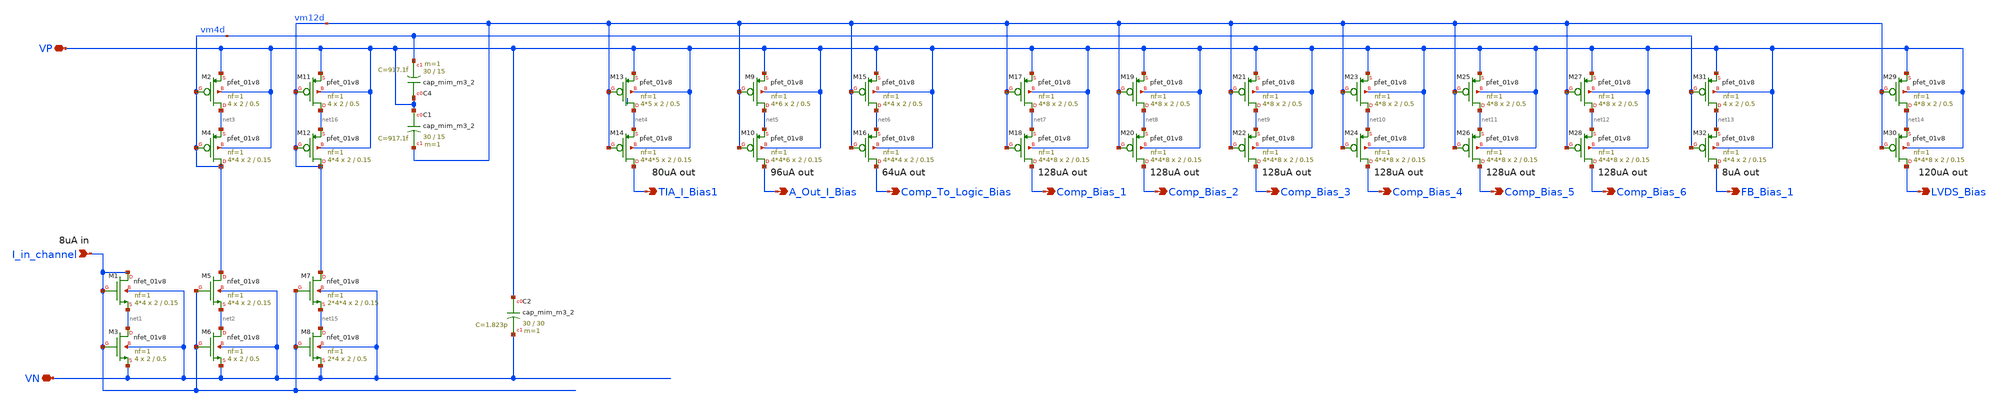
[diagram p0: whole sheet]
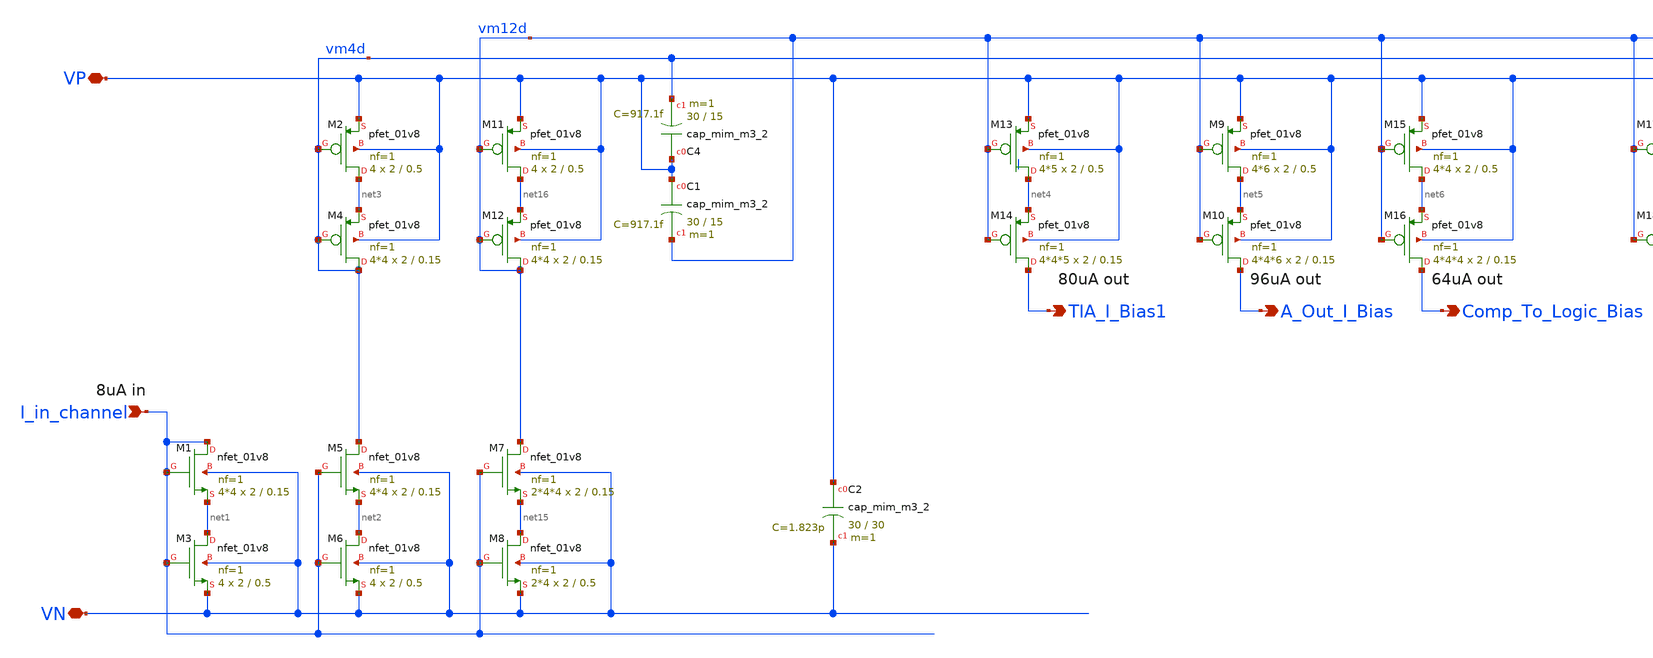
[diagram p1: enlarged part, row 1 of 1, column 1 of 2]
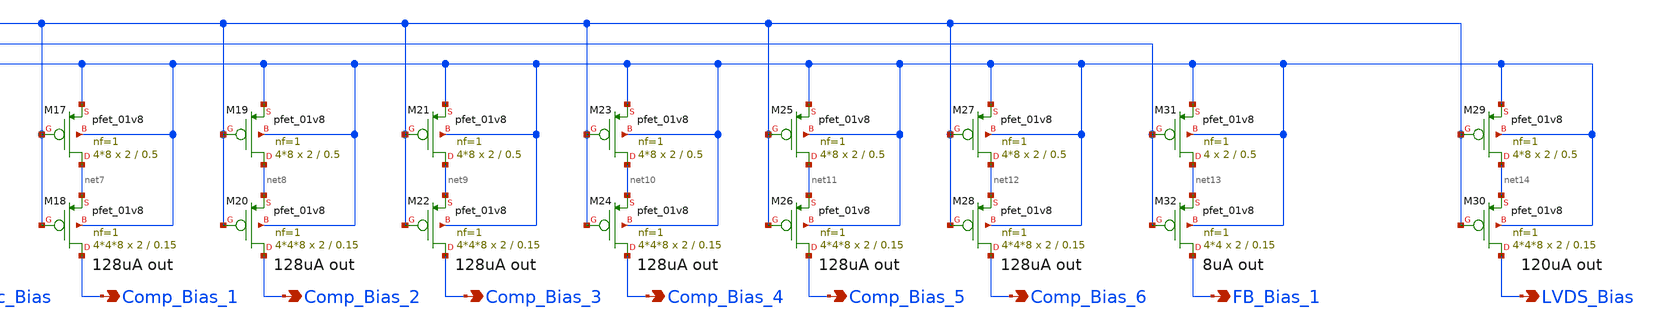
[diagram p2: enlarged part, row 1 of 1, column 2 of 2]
** sch_path: xschem/bias/current_mirror_channel.sch
**.subckt current_mirror_channel I_in_channel VP VN TIA_I_Bias1 A_Out_I_Bias Comp_Bias_1
*+ Comp_To_Logic_Bias Comp_Bias_2 Comp_Bias_3 Comp_Bias_4 Comp_Bias_5 Comp_Bias_6 FB_Bias_1 LVDS_Bias
*.ipin I_in_channel
*.iopin VP
*.iopin VN
*.opin TIA_I_Bias1
*.opin A_Out_I_Bias
*.opin Comp_Bias_1
*.opin Comp_To_Logic_Bias
*.opin Comp_Bias_2
*.opin Comp_Bias_3
*.opin Comp_Bias_4
*.opin Comp_Bias_5
*.opin Comp_Bias_6
*.opin FB_Bias_1
*.opin LVDS_Bias
XM1 I_in_channel I_in_channel net1 VN sky130_fd_pr__nfet_01v8 L=0.15 W=2 nf=1 ad='int((nf+1)/2) * W/nf * 0.29'
+ as='int((nf+2)/2) * W/nf * 0.29' pd='2*int((nf+1)/2) * (W/nf + 0.29)' ps='2*int((nf+2)/2) * (W/nf + 0.29)'
+ nrd='0.29 / W' nrs='0.29 / W' sa=0 sb=0 sd=0 mult=4*4 m=4*4
XM2 net3 vm4d VP VP sky130_fd_pr__pfet_01v8 L=0.5 W=2 nf=1 ad='int((nf+1)/2) * W/nf * 0.29' as='int((nf+2)/2) * W/nf * 0.29'
+ pd='2*int((nf+1)/2) * (W/nf + 0.29)' ps='2*int((nf+2)/2) * (W/nf + 0.29)' nrd='0.29 / W' nrs='0.29 / W'
+ sa=0 sb=0 sd=0 mult=4 m=4
XM3 net1 I_in_channel VN VN sky130_fd_pr__nfet_01v8 L=0.5 W=2 nf=1 ad='int((nf+1)/2) * W/nf * 0.29' as='int((nf+2)/2) * W/nf * 0.29'
+ pd='2*int((nf+1)/2) * (W/nf + 0.29)' ps='2*int((nf+2)/2) * (W/nf + 0.29)' nrd='0.29 / W' nrs='0.29 / W'
+ sa=0 sb=0 sd=0 mult=4 m=4
XM4 vm4d vm4d net3 VP sky130_fd_pr__pfet_01v8 L=0.15 W=2 nf=1 ad='int((nf+1)/2) * W/nf * 0.29' as='int((nf+2)/2) * W/nf * 0.29'
+ pd='2*int((nf+1)/2) * (W/nf + 0.29)' ps='2*int((nf+2)/2) * (W/nf + 0.29)' nrd='0.29 / W' nrs='0.29 / W'
+ sa=0 sb=0 sd=0 mult=4*4 m=4*4
XC4 VP vm4d sky130_fd_pr__cap_mim_m3_2 W=30 L=15 MF=1 m=1
XM5 vm4d I_in_channel net2 VN sky130_fd_pr__nfet_01v8 L=0.15 W=2 nf=1 ad='int((nf+1)/2) * W/nf * 0.29'
+ as='int((nf+2)/2) * W/nf * 0.29' pd='2*int((nf+1)/2) * (W/nf + 0.29)' ps='2*int((nf+2)/2) * (W/nf + 0.29)'
+ nrd='0.29 / W' nrs='0.29 / W' sa=0 sb=0 sd=0 mult=4*4 m=4*4
XM6 net2 I_in_channel VN VN sky130_fd_pr__nfet_01v8 L=0.5 W=2 nf=1 ad='int((nf+1)/2) * W/nf * 0.29' as='int((nf+2)/2) * W/nf * 0.29'
+ pd='2*int((nf+1)/2) * (W/nf + 0.29)' ps='2*int((nf+2)/2) * (W/nf + 0.29)' nrd='0.29 / W' nrs='0.29 / W'
+ sa=0 sb=0 sd=0 mult=4 m=4
XM13 net4 vm12d VP VP sky130_fd_pr__pfet_01v8 L=0.5 W=2 nf=1 ad='int((nf+1)/2) * W/nf * 0.29' as='int((nf+2)/2) * W/nf * 0.29'
+ pd='2*int((nf+1)/2) * (W/nf + 0.29)' ps='2*int((nf+2)/2) * (W/nf + 0.29)' nrd='0.29 / W' nrs='0.29 / W'
+ sa=0 sb=0 sd=0 mult=4*5 m=4*5
XM14 TIA_I_Bias1 vm12d net4 VP sky130_fd_pr__pfet_01v8 L=0.15 W=2 nf=1 ad='int((nf+1)/2) * W/nf * 0.29'
+ as='int((nf+2)/2) * W/nf * 0.29' pd='2*int((nf+1)/2) * (W/nf + 0.29)' ps='2*int((nf+2)/2) * (W/nf + 0.29)'
+ nrd='0.29 / W' nrs='0.29 / W' sa=0 sb=0 sd=0 mult=4*4*5 m=4*4*5
XM9 net5 vm12d VP VP sky130_fd_pr__pfet_01v8 L=0.5 W=2 nf=1 ad='int((nf+1)/2) * W/nf * 0.29' as='int((nf+2)/2) * W/nf * 0.29'
+ pd='2*int((nf+1)/2) * (W/nf + 0.29)' ps='2*int((nf+2)/2) * (W/nf + 0.29)' nrd='0.29 / W' nrs='0.29 / W'
+ sa=0 sb=0 sd=0 mult=4*6 m=4*6
XM10 A_Out_I_Bias vm12d net5 VP sky130_fd_pr__pfet_01v8 L=0.15 W=2 nf=1 ad='int((nf+1)/2) * W/nf * 0.29'
+ as='int((nf+2)/2) * W/nf * 0.29' pd='2*int((nf+1)/2) * (W/nf + 0.29)' ps='2*int((nf+2)/2) * (W/nf + 0.29)'
+ nrd='0.29 / W' nrs='0.29 / W' sa=0 sb=0 sd=0 mult=4*4*6 m=4*4*6
XM15 net6 vm12d VP VP sky130_fd_pr__pfet_01v8 L=0.5 W=2 nf=1 ad='int((nf+1)/2) * W/nf * 0.29' as='int((nf+2)/2) * W/nf * 0.29'
+ pd='2*int((nf+1)/2) * (W/nf + 0.29)' ps='2*int((nf+2)/2) * (W/nf + 0.29)' nrd='0.29 / W' nrs='0.29 / W'
+ sa=0 sb=0 sd=0 mult=4*4 m=4*4
XM16 Comp_To_Logic_Bias vm12d net6 VP sky130_fd_pr__pfet_01v8 L=0.15 W=2 nf=1 ad='int((nf+1)/2) * W/nf * 0.29'
+ as='int((nf+2)/2) * W/nf * 0.29' pd='2*int((nf+1)/2) * (W/nf + 0.29)' ps='2*int((nf+2)/2) * (W/nf + 0.29)'
+ nrd='0.29 / W' nrs='0.29 / W' sa=0 sb=0 sd=0 mult=4*4*4 m=4*4*4
XM17 net7 vm12d VP VP sky130_fd_pr__pfet_01v8 L=0.5 W=2 nf=1 ad='int((nf+1)/2) * W/nf * 0.29' as='int((nf+2)/2) * W/nf * 0.29'
+ pd='2*int((nf+1)/2) * (W/nf + 0.29)' ps='2*int((nf+2)/2) * (W/nf + 0.29)' nrd='0.29 / W' nrs='0.29 / W'
+ sa=0 sb=0 sd=0 mult=4*8 m=4*8
XM18 Comp_Bias_1 vm12d net7 VP sky130_fd_pr__pfet_01v8 L=0.15 W=2 nf=1 ad='int((nf+1)/2) * W/nf * 0.29'
+ as='int((nf+2)/2) * W/nf * 0.29' pd='2*int((nf+1)/2) * (W/nf + 0.29)' ps='2*int((nf+2)/2) * (W/nf + 0.29)'
+ nrd='0.29 / W' nrs='0.29 / W' sa=0 sb=0 sd=0 mult=4*4*8 m=4*4*8
XM19 net8 vm12d VP VP sky130_fd_pr__pfet_01v8 L=0.5 W=2 nf=1 ad='int((nf+1)/2) * W/nf * 0.29' as='int((nf+2)/2) * W/nf * 0.29'
+ pd='2*int((nf+1)/2) * (W/nf + 0.29)' ps='2*int((nf+2)/2) * (W/nf + 0.29)' nrd='0.29 / W' nrs='0.29 / W'
+ sa=0 sb=0 sd=0 mult=4*8 m=4*8
XM20 Comp_Bias_2 vm12d net8 VP sky130_fd_pr__pfet_01v8 L=0.15 W=2 nf=1 ad='int((nf+1)/2) * W/nf * 0.29'
+ as='int((nf+2)/2) * W/nf * 0.29' pd='2*int((nf+1)/2) * (W/nf + 0.29)' ps='2*int((nf+2)/2) * (W/nf + 0.29)'
+ nrd='0.29 / W' nrs='0.29 / W' sa=0 sb=0 sd=0 mult=4*4*8 m=4*4*8
XM31 net13 vm4d VP VP sky130_fd_pr__pfet_01v8 L=0.5 W=2 nf=1 ad='int((nf+1)/2) * W/nf * 0.29' as='int((nf+2)/2) * W/nf * 0.29'
+ pd='2*int((nf+1)/2) * (W/nf + 0.29)' ps='2*int((nf+2)/2) * (W/nf + 0.29)' nrd='0.29 / W' nrs='0.29 / W'
+ sa=0 sb=0 sd=0 mult=4 m=4
XM32 FB_Bias_1 vm4d net13 VP sky130_fd_pr__pfet_01v8 L=0.15 W=2 nf=1 ad='int((nf+1)/2) * W/nf * 0.29'
+ as='int((nf+2)/2) * W/nf * 0.29' pd='2*int((nf+1)/2) * (W/nf + 0.29)' ps='2*int((nf+2)/2) * (W/nf + 0.29)'
+ nrd='0.29 / W' nrs='0.29 / W' sa=0 sb=0 sd=0 mult=4*4 m=4*4
XM7 vm12d I_in_channel net15 VN sky130_fd_pr__nfet_01v8 L=0.15 W=2 nf=1 ad='int((nf+1)/2) * W/nf * 0.29'
+ as='int((nf+2)/2) * W/nf * 0.29' pd='2*int((nf+1)/2) * (W/nf + 0.29)' ps='2*int((nf+2)/2) * (W/nf + 0.29)'
+ nrd='0.29 / W' nrs='0.29 / W' sa=0 sb=0 sd=0 mult=2*4*4 m=2*4*4
XM8 net15 I_in_channel VN VN sky130_fd_pr__nfet_01v8 L=0.5 W=2 nf=1 ad='int((nf+1)/2) * W/nf * 0.29'
+ as='int((nf+2)/2) * W/nf * 0.29' pd='2*int((nf+1)/2) * (W/nf + 0.29)' ps='2*int((nf+2)/2) * (W/nf + 0.29)'
+ nrd='0.29 / W' nrs='0.29 / W' sa=0 sb=0 sd=0 mult=2*4 m=2*4
XM11 net16 vm12d VP VP sky130_fd_pr__pfet_01v8 L=0.5 W=2 nf=1 ad='int((nf+1)/2) * W/nf * 0.29' as='int((nf+2)/2) * W/nf * 0.29'
+ pd='2*int((nf+1)/2) * (W/nf + 0.29)' ps='2*int((nf+2)/2) * (W/nf + 0.29)' nrd='0.29 / W' nrs='0.29 / W'
+ sa=0 sb=0 sd=0 mult=4 m=4
XM12 vm12d vm12d net16 VP sky130_fd_pr__pfet_01v8 L=0.15 W=2 nf=1 ad='int((nf+1)/2) * W/nf * 0.29' as='int((nf+2)/2) * W/nf * 0.29'
+ pd='2*int((nf+1)/2) * (W/nf + 0.29)' ps='2*int((nf+2)/2) * (W/nf + 0.29)' nrd='0.29 / W' nrs='0.29 / W'
+ sa=0 sb=0 sd=0 mult=4*4 m=4*4
XM21 net9 vm12d VP VP sky130_fd_pr__pfet_01v8 L=0.5 W=2 nf=1 ad='int((nf+1)/2) * W/nf * 0.29' as='int((nf+2)/2) * W/nf * 0.29'
+ pd='2*int((nf+1)/2) * (W/nf + 0.29)' ps='2*int((nf+2)/2) * (W/nf + 0.29)' nrd='0.29 / W' nrs='0.29 / W'
+ sa=0 sb=0 sd=0 mult=4*8 m=4*8
XM22 Comp_Bias_3 vm12d net9 VP sky130_fd_pr__pfet_01v8 L=0.15 W=2 nf=1 ad='int((nf+1)/2) * W/nf * 0.29'
+ as='int((nf+2)/2) * W/nf * 0.29' pd='2*int((nf+1)/2) * (W/nf + 0.29)' ps='2*int((nf+2)/2) * (W/nf + 0.29)'
+ nrd='0.29 / W' nrs='0.29 / W' sa=0 sb=0 sd=0 mult=4*4*8 m=4*4*8
XM23 net10 vm12d VP VP sky130_fd_pr__pfet_01v8 L=0.5 W=2 nf=1 ad='int((nf+1)/2) * W/nf * 0.29' as='int((nf+2)/2) * W/nf * 0.29'
+ pd='2*int((nf+1)/2) * (W/nf + 0.29)' ps='2*int((nf+2)/2) * (W/nf + 0.29)' nrd='0.29 / W' nrs='0.29 / W'
+ sa=0 sb=0 sd=0 mult=4*8 m=4*8
XM24 Comp_Bias_4 vm12d net10 VP sky130_fd_pr__pfet_01v8 L=0.15 W=2 nf=1 ad='int((nf+1)/2) * W/nf * 0.29'
+ as='int((nf+2)/2) * W/nf * 0.29' pd='2*int((nf+1)/2) * (W/nf + 0.29)' ps='2*int((nf+2)/2) * (W/nf + 0.29)'
+ nrd='0.29 / W' nrs='0.29 / W' sa=0 sb=0 sd=0 mult=4*4*8 m=4*4*8
XM25 net11 vm12d VP VP sky130_fd_pr__pfet_01v8 L=0.5 W=2 nf=1 ad='int((nf+1)/2) * W/nf * 0.29' as='int((nf+2)/2) * W/nf * 0.29'
+ pd='2*int((nf+1)/2) * (W/nf + 0.29)' ps='2*int((nf+2)/2) * (W/nf + 0.29)' nrd='0.29 / W' nrs='0.29 / W'
+ sa=0 sb=0 sd=0 mult=4*8 m=4*8
XM26 Comp_Bias_5 vm12d net11 VP sky130_fd_pr__pfet_01v8 L=0.15 W=2 nf=1 ad='int((nf+1)/2) * W/nf * 0.29'
+ as='int((nf+2)/2) * W/nf * 0.29' pd='2*int((nf+1)/2) * (W/nf + 0.29)' ps='2*int((nf+2)/2) * (W/nf + 0.29)'
+ nrd='0.29 / W' nrs='0.29 / W' sa=0 sb=0 sd=0 mult=4*4*8 m=4*4*8
XM27 net12 vm12d VP VP sky130_fd_pr__pfet_01v8 L=0.5 W=2 nf=1 ad='int((nf+1)/2) * W/nf * 0.29' as='int((nf+2)/2) * W/nf * 0.29'
+ pd='2*int((nf+1)/2) * (W/nf + 0.29)' ps='2*int((nf+2)/2) * (W/nf + 0.29)' nrd='0.29 / W' nrs='0.29 / W'
+ sa=0 sb=0 sd=0 mult=4*8 m=4*8
XM28 Comp_Bias_6 vm12d net12 VP sky130_fd_pr__pfet_01v8 L=0.15 W=2 nf=1 ad='int((nf+1)/2) * W/nf * 0.29'
+ as='int((nf+2)/2) * W/nf * 0.29' pd='2*int((nf+1)/2) * (W/nf + 0.29)' ps='2*int((nf+2)/2) * (W/nf + 0.29)'
+ nrd='0.29 / W' nrs='0.29 / W' sa=0 sb=0 sd=0 mult=4*4*8 m=4*4*8
XM29 net14 vm12d VP VP sky130_fd_pr__pfet_01v8 L=0.5 W=2 nf=1 ad='int((nf+1)/2) * W/nf * 0.29' as='int((nf+2)/2) * W/nf * 0.29'
+ pd='2*int((nf+1)/2) * (W/nf + 0.29)' ps='2*int((nf+2)/2) * (W/nf + 0.29)' nrd='0.29 / W' nrs='0.29 / W'
+ sa=0 sb=0 sd=0 mult=4*8 m=4*8
XM30 LVDS_Bias vm12d net14 VP sky130_fd_pr__pfet_01v8 L=0.15 W=2 nf=1 ad='int((nf+1)/2) * W/nf * 0.29'
+ as='int((nf+2)/2) * W/nf * 0.29' pd='2*int((nf+1)/2) * (W/nf + 0.29)' ps='2*int((nf+2)/2) * (W/nf + 0.29)'
+ nrd='0.29 / W' nrs='0.29 / W' sa=0 sb=0 sd=0 mult=4*4*8 m=4*4*8
XC1 VP vm12d sky130_fd_pr__cap_mim_m3_2 W=30 L=15 MF=1 m=1
XC2 VP VN sky130_fd_pr__cap_mim_m3_2 W=30 L=30 MF=1 m=1
**.ends
.end
